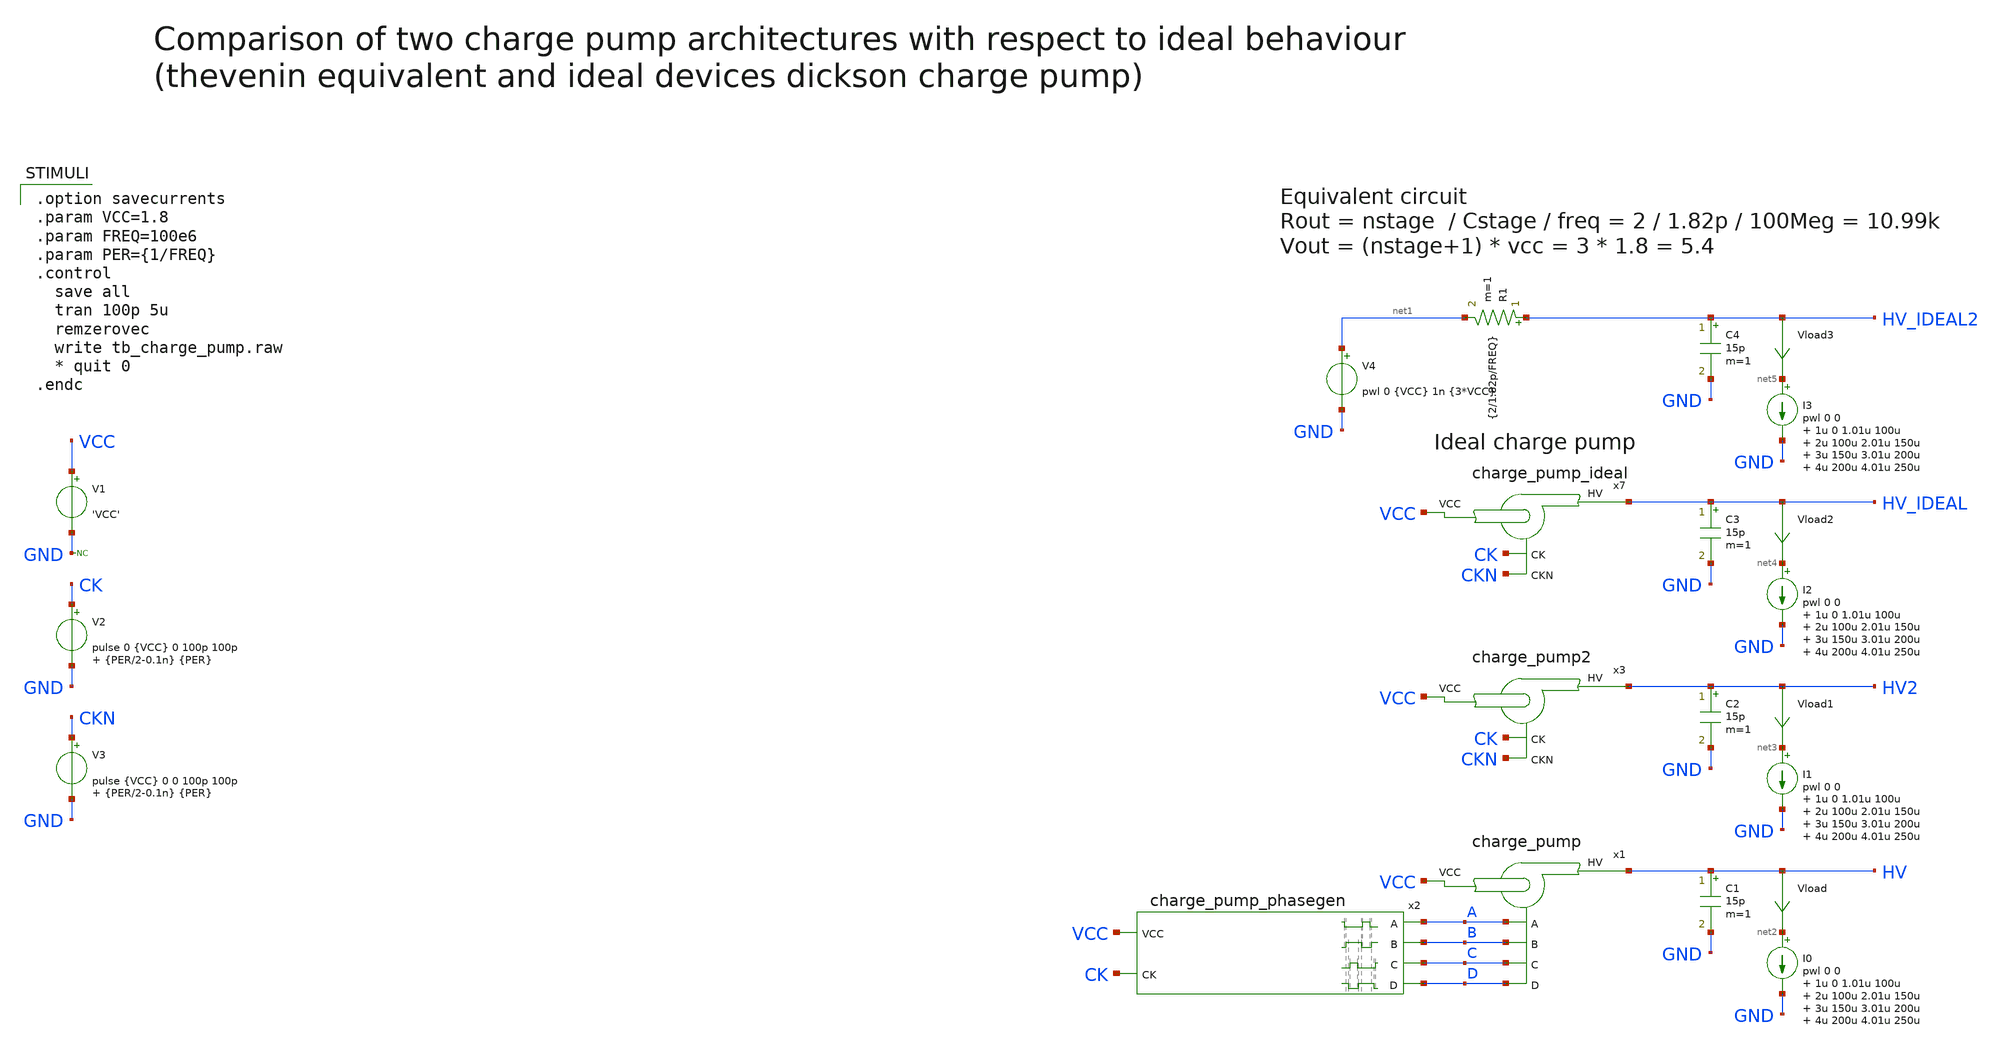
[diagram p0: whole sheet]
** sch_path: sky130_tests/tb_charge_pump.sch
* Copyright 2021 Stefan Frederik Schippers
* Licensed under the Apache License, Version 2.0 (the "License");
* you may not use this file except in compliance with the License.
* You may obtain a copy of the License at
* https://www.apache.org/licenses/LICENSE-2.0
* Unless required by applicable law or agreed to in writing, software
* distributed under the License is distributed on an "AS IS" BASIS,
* WITHOUT WARRANTIES OR CONDITIONS OF ANY KIND, either express or implied.
* See the License for the specific language governing permissions and
* limitations under the License.
* sky130_tests/lvtnot.sch:
* Copyright 2020 Stefan Frederik Schippers
.lib $::SKYWATER_MODELS/sky130.lib.spice tt
.include $::SKYWATER_STDCELLS/sky130_fd_sc_hd.spice

**.subckt tb_charge_pump
x1 VCC HV A B C D charge_pump
x2 A B C CK D VCC charge_pump_phasegen
V1 VCC GND 'VCC'
V2 CK GND pulse 0 {VCC} 0 100p 100p {PER/2-0.1n} {PER}
C1 HV GND 15p m=1
I0 net2 GND pwl 0 0 1u 0 1.01u 100u 2u 100u 2.01u 150u 3u 150u 3.01u 200u 4u 200u 4.01u 250u
Vload HV net2 0
.save i(vload)
x3 VCC HV2 CK CKN charge_pump2
V3 CKN GND pulse {VCC} 0 0 100p 100p {PER/2-0.1n} {PER}
C2 HV2 GND 15p m=1
I1 net3 GND pwl 0 0 1u 0 1.01u 100u 2u 100u 2.01u 150u 3u 150u 3.01u 200u 4u 200u 4.01u 250u
Vload1 HV2 net3 0
.save i(vload1)
* noconn GND
C3 HV_IDEAL GND 15p m=1
Vload2 HV_IDEAL net4 0
.save i(vload2)
x7 VCC HV_IDEAL CK CKN charge_pump_ideal
I2 net4 GND pwl 0 0 1u 0 1.01u 100u 2u 100u 2.01u 150u 3u 150u 3.01u 200u 4u 200u 4.01u 250u
V4 net1 GND pwl 0 {VCC} 1n {3*VCC}
R1 HV_IDEAL2 net1 {2/1.82p/FREQ} m=1
C4 HV_IDEAL2 GND 15p m=1
Vload3 HV_IDEAL2 net5 0
.save i(vload3)
I3 net5 GND pwl 0 0 1u 0 1.01u 100u 2u 100u 2.01u 150u 3u 150u 3.01u 200u 4u 200u 4.01u 250u
**** begin user architecture code

.option savecurrents
.param VCC=1.8
.param FREQ=100e6
.param PER={1/FREQ}
.control
  save all
  tran 100p 5u
  remzerovec
  write tb_charge_pump.raw
  * quit 0
.endc


**** end user architecture code
**.ends

* expanding   symbol:  sky130_tests/charge_pump.sym # of pins=6
** sym_path: sky130_tests/charge_pump.sym
** sch_path: sky130_tests/charge_pump.sch
.subckt charge_pump VCC HV A B C D
*.ipin A
*.ipin B
*.ipin C
*.ipin D
*.ipin VCC
*.iopin HV
XM1 net15 net9 net16 net5 sky130_fd_pr__nfet_g5v0d10v5 L=0.5 W=8 nf=1 ad='int((1 + 1)/2) * 8 / 1 * 0.29'
+ as='int((1 + 2)/2) * 8 / 1 * 0.29' pd='2*int((1 + 1)/2) * (8 / 1 + 0.29)' ps='2*int((1 + 2)/2) * (8 / 1 + 0.29)'
+ nrd='0.29 / 8 ' nrs='0.29 / 8 ' sa=0 sb=0 sd=0 mult=1 m=1
XM2 VCC HV1A G1A VCC sky130_fd_pr__nfet_g5v0d10v5 L=0.5 W=1.5 nf=1 ad='int((1 + 1)/2) * 1.5 / 1 * 0.29'
+ as='int((1 + 2)/2) * 1.5 / 1 * 0.29' pd='2*int((1 + 1)/2) * (1.5 / 1 + 0.29)' ps='2*int((1 + 2)/2) * (1.5 / 1 + 0.29)'
+ nrd='0.29 / 1.5 ' nrs='0.29 / 1.5 ' sa=0 sb=0 sd=0 mult=1 m=1
XM3 net1 net10 net17 net6 sky130_fd_pr__nfet_g5v0d10v5 L=0.5 W=8 nf=1 ad='int((1 + 1)/2) * 8 / 1 * 0.29'
+ as='int((1 + 2)/2) * 8 / 1 * 0.29' pd='2*int((1 + 1)/2) * (8 / 1 + 0.29)' ps='2*int((1 + 2)/2) * (8 / 1 + 0.29)'
+ nrd='0.29 / 8 ' nrs='0.29 / 8 ' sa=0 sb=0 sd=0 mult=1 m=1
XM4 HV1A HV2A G2A HV1A sky130_fd_pr__nfet_g5v0d10v5 L=0.5 W=1.5 nf=1 ad='int((1 + 1)/2) * 1.5 / 1 * 0.29'
+ as='int((1 + 2)/2) * 1.5 / 1 * 0.29' pd='2*int((1 + 1)/2) * (1.5 / 1 + 0.29)' ps='2*int((1 + 2)/2) * (1.5 / 1 + 0.29)'
+ nrd='0.29 / 1.5 ' nrs='0.29 / 1.5 ' sa=0 sb=0 sd=0 mult=1 m=1
XM5 HV2A net11 HV3A HV2A sky130_fd_pr__nfet_g5v0d10v5 L=0.5 W=1.5 nf=1 ad='int((1 + 1)/2) * 1.5 / 1 * 0.29'
+ as='int((1 + 2)/2) * 1.5 / 1 * 0.29' pd='2*int((1 + 1)/2) * (1.5 / 1 + 0.29)' ps='2*int((1 + 2)/2) * (1.5 / 1 + 0.29)'
+ nrd='0.29 / 1.5 ' nrs='0.29 / 1.5 ' sa=0 sb=0 sd=0 mult=1 m=1
XM6 HV2A HV3A G3A HV2A sky130_fd_pr__nfet_g5v0d10v5 L=0.5 W=1.5 nf=1 ad='int((1 + 1)/2) * 1.5 / 1 * 0.29'
+ as='int((1 + 2)/2) * 1.5 / 1 * 0.29' pd='2*int((1 + 1)/2) * (1.5 / 1 + 0.29)' ps='2*int((1 + 2)/2) * (1.5 / 1 + 0.29)'
+ nrd='0.29 / 1.5 ' nrs='0.29 / 1.5 ' sa=0 sb=0 sd=0 mult=1 m=1
XM7 HV2A G3A net3 HV2A sky130_fd_pr__nfet_g5v0d10v5 L=0.5 W=8 nf=1 ad='int((1 + 1)/2) * 8 / 1 * 0.29'
+ as='int((1 + 2)/2) * 8 / 1 * 0.29' pd='2*int((1 + 1)/2) * (8 / 1 + 0.29)' ps='2*int((1 + 2)/2) * (8 / 1 + 0.29)'
+ nrd='0.29 / 8 ' nrs='0.29 / 8 ' sa=0 sb=0 sd=0 mult=1 m=1
XC1 G1A A sky130_fd_pr__cap_mim_m3_1 W=6 L=4 MF=1 m=1
XC2 HV1A B sky130_fd_pr__cap_mim_m3_1 W=30 L=15 MF=1 m=1
XC3 G2A C sky130_fd_pr__cap_mim_m3_1 W=6 L=4 MF=1 m=1
XC4 HV2A D sky130_fd_pr__cap_mim_m3_1 W=30 L=15 MF=1 m=1
XC5 G3A A sky130_fd_pr__cap_mim_m3_1 W=6 L=4 MF=1 m=1
XC6 HV3A B sky130_fd_pr__cap_mim_m3_1 W=6 L=4 MF=1 m=1
XM8 net18 net12 net19 net7 sky130_fd_pr__nfet_g5v0d10v5 L=0.5 W=8 nf=1 ad='int((1 + 1)/2) * 8 / 1 * 0.29'
+ as='int((1 + 2)/2) * 8 / 1 * 0.29' pd='2*int((1 + 1)/2) * (8 / 1 + 0.29)' ps='2*int((1 + 2)/2) * (8 / 1 + 0.29)'
+ nrd='0.29 / 8 ' nrs='0.29 / 8 ' sa=0 sb=0 sd=0 mult=1 m=1
XM9 VCC HV1B G1B VCC sky130_fd_pr__nfet_g5v0d10v5 L=0.5 W=1.5 nf=1 ad='int((1 + 1)/2) * 1.5 / 1 * 0.29'
+ as='int((1 + 2)/2) * 1.5 / 1 * 0.29' pd='2*int((1 + 1)/2) * (1.5 / 1 + 0.29)' ps='2*int((1 + 2)/2) * (1.5 / 1 + 0.29)'
+ nrd='0.29 / 1.5 ' nrs='0.29 / 1.5 ' sa=0 sb=0 sd=0 mult=1 m=1
XM10 net2 net13 net20 net8 sky130_fd_pr__nfet_g5v0d10v5 L=0.5 W=8 nf=1 ad='int((1 + 1)/2) * 8 / 1 * 0.29'
+ as='int((1 + 2)/2) * 8 / 1 * 0.29' pd='2*int((1 + 1)/2) * (8 / 1 + 0.29)' ps='2*int((1 + 2)/2) * (8 / 1 + 0.29)'
+ nrd='0.29 / 8 ' nrs='0.29 / 8 ' sa=0 sb=0 sd=0 mult=1 m=1
XM11 HV1B HV2B G2B HV1B sky130_fd_pr__nfet_g5v0d10v5 L=0.5 W=1.5 nf=1 ad='int((1 + 1)/2) * 1.5 / 1 * 0.29'
+ as='int((1 + 2)/2) * 1.5 / 1 * 0.29' pd='2*int((1 + 1)/2) * (1.5 / 1 + 0.29)' ps='2*int((1 + 2)/2) * (1.5 / 1 + 0.29)'
+ nrd='0.29 / 1.5 ' nrs='0.29 / 1.5 ' sa=0 sb=0 sd=0 mult=1 m=1
XM12 HV2B net14 HV3B HV2B sky130_fd_pr__nfet_g5v0d10v5 L=0.5 W=1.5 nf=1 ad='int((1 + 1)/2) * 1.5 / 1 * 0.29'
+ as='int((1 + 2)/2) * 1.5 / 1 * 0.29' pd='2*int((1 + 1)/2) * (1.5 / 1 + 0.29)' ps='2*int((1 + 2)/2) * (1.5 / 1 + 0.29)'
+ nrd='0.29 / 1.5 ' nrs='0.29 / 1.5 ' sa=0 sb=0 sd=0 mult=1 m=1
XM13 HV2B HV3B G3B HV2B sky130_fd_pr__nfet_g5v0d10v5 L=0.5 W=1.5 nf=1 ad='int((1 + 1)/2) * 1.5 / 1 * 0.29'
+ as='int((1 + 2)/2) * 1.5 / 1 * 0.29' pd='2*int((1 + 1)/2) * (1.5 / 1 + 0.29)' ps='2*int((1 + 2)/2) * (1.5 / 1 + 0.29)'
+ nrd='0.29 / 1.5 ' nrs='0.29 / 1.5 ' sa=0 sb=0 sd=0 mult=1 m=1
XM14 HV2B G3B net4 HV2B sky130_fd_pr__nfet_g5v0d10v5 L=0.5 W=8 nf=1 ad='int((1 + 1)/2) * 8 / 1 * 0.29'
+ as='int((1 + 2)/2) * 8 / 1 * 0.29' pd='2*int((1 + 1)/2) * (8 / 1 + 0.29)' ps='2*int((1 + 2)/2) * (8 / 1 + 0.29)'
+ nrd='0.29 / 8 ' nrs='0.29 / 8 ' sa=0 sb=0 sd=0 mult=1 m=1
XC7 G1B C sky130_fd_pr__cap_mim_m3_1 W=6 L=4 MF=1 m=1
XC8 HV1B D sky130_fd_pr__cap_mim_m3_1 W=30 L=15 MF=1 m=1
XC9 G2B A sky130_fd_pr__cap_mim_m3_1 W=6 L=4 MF=1 m=1
XC10 HV2B B sky130_fd_pr__cap_mim_m3_1 W=30 L=15 MF=1 m=1
XC11 G3B C sky130_fd_pr__cap_mim_m3_1 W=6 L=4 MF=1 m=1
XC12 HV3B D sky130_fd_pr__cap_mim_m3_1 W=6 L=4 MF=1 m=1
V1 HV1B net2 0
.save i(v1)
V2 net3 HV 0
.save i(v2)
V3 net4 HV 0
.save i(v3)
V4 HV1A net1 0
.save i(v4)
V5 VCC net18 0
.save i(v5)
V6 VCC net15 0
.save i(v6)
V7 net20 HV2B 0
.save i(v7)
V8 net17 HV2A 0
.save i(v8)
V9 VCC net5 0
.save i(v9)
V10 HV1A net6 0
.save i(v10)
V11 VCC net7 0
.save i(v11)
V12 HV1B net8 0
.save i(v12)
V13 net19 HV1B 0
.save i(v13)
V14 net16 HV1A 0
.save i(v14)
V15 G1A net9 0
.save i(v15)
V16 G2A net10 0
.save i(v16)
V17 G3A net11 0
.save i(v17)
V18 G1B net12 0
.save i(v18)
V19 G2B net13 0
.save i(v19)
V20 G3B net14 0
.save i(v20)
.ends


* expanding   symbol:  sky130_tests/charge_pump_phasegen.sym # of pins=6
** sym_path: sky130_tests/charge_pump_phasegen.sym
** sch_path: sky130_tests/charge_pump_phasegen.sch
.subckt charge_pump_phasegen A B C CK D VCC
*.ipin CK
*.opin A
*.opin B
*.opin C
*.opin D
*.ipin VCC
x1 CKN BN GND GND VCC VCC AN sky130_fd_sc_hd__nand2_2
x2 AN GND GND VCC VCC A sky130_fd_sc_hd__inv_4
x5 AN CK GND GND VCC VCC net1 sky130_fd_sc_hd__nand2_1
x6 net1 net2 GND GND VCC VCC net5 sky130_fd_sc_hd__nand2_1
x7 net6 DI VCC GND lvtnot W_N=0.5 L_N=1 W_P=1 L_P=1 m=1
x8 net2 net6 VCC GND lvtnot W_N=0.5 L_N=1 W_P=1 L_P=1 m=1
x9 BN GND GND VCC VCC B sky130_fd_sc_hd__inv_12
x10 net5 GND GND VCC VCC BN sky130_fd_sc_hd__inv_2
x11 CK DN GND GND VCC VCC CN sky130_fd_sc_hd__nand2_2
x12 CN GND GND VCC VCC C sky130_fd_sc_hd__inv_4
x13 CN CKN GND GND VCC VCC net3 sky130_fd_sc_hd__nand2_1
x14 net3 net4 GND GND VCC VCC net7 sky130_fd_sc_hd__nand2_1
x15 net8 BI VCC GND lvtnot W_N=0.5 L_N=1 W_P=1 L_P=1 m=1
x16 net4 net8 VCC GND lvtnot W_N=0.5 L_N=1 W_P=1 L_P=1 m=1
x17 DN GND GND VCC VCC D sky130_fd_sc_hd__inv_12
x18 net7 GND GND VCC VCC DN sky130_fd_sc_hd__inv_2
x3 CK GND GND VCC VCC CKN sky130_fd_sc_hd__inv_12
* noconn VCC
x19 BN GND GND VCC VCC BI sky130_fd_sc_hd__inv_2
x20 DN GND GND VCC VCC DI sky130_fd_sc_hd__inv_2
.ends


* expanding   symbol:  sky130_tests/charge_pump2.sym # of pins=4
** sym_path: sky130_tests/charge_pump2.sym
** sch_path: sky130_tests/charge_pump2.sch
.subckt charge_pump2 VCC HV CK CKN
*.ipin VCC
*.iopin HV
*.ipin CK
*.ipin CKN
XM8 D1 GN1 VCC VCC sky130_fd_pr__nfet_g5v0d10v5 L=0.5 W=8 nf=1 ad='int((1 + 1)/2) * 8 / 1 * 0.29' as='int((1 + 2)/2) * 8 / 1 * 0.29'
+ pd='2*int((1 + 1)/2) * (8 / 1 + 0.29)' ps='2*int((1 + 2)/2) * (8 / 1 + 0.29)' nrd='0.29 / 8 ' nrs='0.29 / 8 '
+ sa=0 sb=0 sd=0 mult=1 m=1
XM9 D2 GN2 VCC VCC sky130_fd_pr__nfet_g5v0d10v5 L=0.5 W=8 nf=1 ad='int((1 + 1)/2) * 8 / 1 * 0.29' as='int((1 + 2)/2) * 8 / 1 * 0.29'
+ pd='2*int((1 + 1)/2) * (8 / 1 + 0.29)' ps='2*int((1 + 2)/2) * (8 / 1 + 0.29)' nrd='0.29 / 8 ' nrs='0.29 / 8 '
+ sa=0 sb=0 sd=0 mult=1 m=1
XM10 D1 GP1 HV1 HV1 sky130_fd_pr__pfet_g5v0d10v5 L=0.5 W=16 nf=1 ad='int((1 + 1)/2) * 16 / 1 * 0.29'
+ as='int((1 + 2)/2) * 16 / 1 * 0.29' pd='2*int((1 + 1)/2) * (16 / 1 + 0.29)' ps='2*int((1 + 2)/2) * (16 / 1 + 0.29)'
+ nrd='0.29 / 16 ' nrs='0.29 / 16 ' sa=0 sb=0 sd=0 mult=1 m=1
XM11 D2 GP2 HV1 HV1 sky130_fd_pr__pfet_g5v0d10v5 L=0.5 W=16 nf=1 ad='int((1 + 1)/2) * 16 / 1 * 0.29'
+ as='int((1 + 2)/2) * 16 / 1 * 0.29' pd='2*int((1 + 1)/2) * (16 / 1 + 0.29)' ps='2*int((1 + 2)/2) * (16 / 1 + 0.29)'
+ nrd='0.29 / 16 ' nrs='0.29 / 16 ' sa=0 sb=0 sd=0 mult=1 m=1
XC7 D2 net1 sky130_fd_pr__cap_mim_m3_1 W=30 L=15 MF=1 m=1
XC8 D1 net2 sky130_fd_pr__cap_mim_m3_1 W=30 L=15 MF=1 m=1
XM12 D3 GN3 HV1 HV1 sky130_fd_pr__nfet_g5v0d10v5 L=0.5 W=8 nf=1 ad='int((1 + 1)/2) * 8 / 1 * 0.29' as='int((1 + 2)/2) * 8 / 1 * 0.29'
+ pd='2*int((1 + 1)/2) * (8 / 1 + 0.29)' ps='2*int((1 + 2)/2) * (8 / 1 + 0.29)' nrd='0.29 / 8 ' nrs='0.29 / 8 '
+ sa=0 sb=0 sd=0 mult=1 m=1
XM13 D4 GN4 HV1 HV1 sky130_fd_pr__nfet_g5v0d10v5 L=0.5 W=8 nf=1 ad='int((1 + 1)/2) * 8 / 1 * 0.29' as='int((1 + 2)/2) * 8 / 1 * 0.29'
+ pd='2*int((1 + 1)/2) * (8 / 1 + 0.29)' ps='2*int((1 + 2)/2) * (8 / 1 + 0.29)' nrd='0.29 / 8 ' nrs='0.29 / 8 '
+ sa=0 sb=0 sd=0 mult=1 m=1
XM14 D3 GP3 HV HV sky130_fd_pr__pfet_g5v0d10v5 L=0.5 W=16 nf=1 ad='int((1 + 1)/2) * 16 / 1 * 0.29' as='int((1 + 2)/2) * 16 / 1 * 0.29'
+ pd='2*int((1 + 1)/2) * (16 / 1 + 0.29)' ps='2*int((1 + 2)/2) * (16 / 1 + 0.29)' nrd='0.29 / 16 ' nrs='0.29 / 16 '
+ sa=0 sb=0 sd=0 mult=1 m=1
XM15 D4 GP4 HV HV sky130_fd_pr__pfet_g5v0d10v5 L=0.5 W=16 nf=1 ad='int((1 + 1)/2) * 16 / 1 * 0.29' as='int((1 + 2)/2) * 16 / 1 * 0.29'
+ pd='2*int((1 + 1)/2) * (16 / 1 + 0.29)' ps='2*int((1 + 2)/2) * (16 / 1 + 0.29)' nrd='0.29 / 16 ' nrs='0.29 / 16 '
+ sa=0 sb=0 sd=0 mult=1 m=1
XC9 D4 net3 sky130_fd_pr__cap_mim_m3_1 W=30 L=15 MF=1 m=1
XC10 D3 net4 sky130_fd_pr__cap_mim_m3_1 W=30 L=15 MF=1 m=1
x12 CK GND GND VCC VCC net1 sky130_fd_sc_hd__inv_6
x1 CKN GND GND VCC VCC net2 sky130_fd_sc_hd__inv_6
x2 CK GND GND VCC VCC net3 sky130_fd_sc_hd__inv_6
x3 CKN GND GND VCC VCC net4 sky130_fd_sc_hd__inv_6
XM1 GP3 GP4 HV HV sky130_fd_pr__pfet_g5v0d10v5 L=0.5 W=1 nf=1 ad='int((1 + 1)/2) * 1 / 1 * 0.29' as='int((1 + 2)/2) * 1 / 1 * 0.29'
+ pd='2*int((1 + 1)/2) * (1 / 1 + 0.29)' ps='2*int((1 + 2)/2) * (1 / 1 + 0.29)' nrd='0.29 / 1 ' nrs='0.29 / 1 '
+ sa=0 sb=0 sd=0 mult=1 m=1
XM2 GP4 GP3 HV HV sky130_fd_pr__pfet_g5v0d10v5 L=0.5 W=1 nf=1 ad='int((1 + 1)/2) * 1 / 1 * 0.29' as='int((1 + 2)/2) * 1 / 1 * 0.29'
+ pd='2*int((1 + 1)/2) * (1 / 1 + 0.29)' ps='2*int((1 + 2)/2) * (1 / 1 + 0.29)' nrd='0.29 / 1 ' nrs='0.29 / 1 '
+ sa=0 sb=0 sd=0 mult=1 m=1
XC1 GP3 net5 sky130_fd_pr__cap_mim_m3_1 W=6 L=8 MF=1 m=1
XC2 GP4 net6 sky130_fd_pr__cap_mim_m3_1 W=6 L=8 MF=1 m=1
XM3 GP1 GP2 HV1 HV1 sky130_fd_pr__pfet_g5v0d10v5 L=0.5 W=1 nf=1 ad='int((1 + 1)/2) * 1 / 1 * 0.29' as='int((1 + 2)/2) * 1 / 1 * 0.29'
+ pd='2*int((1 + 1)/2) * (1 / 1 + 0.29)' ps='2*int((1 + 2)/2) * (1 / 1 + 0.29)' nrd='0.29 / 1 ' nrs='0.29 / 1 '
+ sa=0 sb=0 sd=0 mult=1 m=1
XM4 GP2 GP1 HV1 HV1 sky130_fd_pr__pfet_g5v0d10v5 L=0.5 W=1 nf=1 ad='int((1 + 1)/2) * 1 / 1 * 0.29' as='int((1 + 2)/2) * 1 / 1 * 0.29'
+ pd='2*int((1 + 1)/2) * (1 / 1 + 0.29)' ps='2*int((1 + 2)/2) * (1 / 1 + 0.29)' nrd='0.29 / 1 ' nrs='0.29 / 1 '
+ sa=0 sb=0 sd=0 mult=1 m=1
XC3 GP1 net7 sky130_fd_pr__cap_mim_m3_1 W=6 L=8 MF=1 m=1
XC4 GP2 net8 sky130_fd_pr__cap_mim_m3_1 W=6 L=8 MF=1 m=1
x4 CK GND GND VCC VCC net5 sky130_fd_sc_hd__inv_2
x5 CKN GND GND VCC VCC net6 sky130_fd_sc_hd__inv_2
x6 CK GND GND VCC VCC net7 sky130_fd_sc_hd__inv_2
x7 CKN GND GND VCC VCC net8 sky130_fd_sc_hd__inv_2
XC5 GN1 net9 sky130_fd_pr__cap_mim_m3_1 W=6 L=4 MF=1 m=1
XC6 GN2 net10 sky130_fd_pr__cap_mim_m3_1 W=6 L=4 MF=1 m=1
x8 CK GND GND VCC VCC net9 sky130_fd_sc_hd__inv_2
x9 CKN GND GND VCC VCC net10 sky130_fd_sc_hd__inv_2
XM5 VCC GN1 GN2 VCC sky130_fd_pr__nfet_g5v0d10v5 L=0.5 W=0.5 nf=1 ad='int((1 + 1)/2) * 0.5 / 1 * 0.29'
+ as='int((1 + 2)/2) * 0.5 / 1 * 0.29' pd='2*int((1 + 1)/2) * (0.5 / 1 + 0.29)' ps='2*int((1 + 2)/2) * (0.5 / 1 + 0.29)'
+ nrd='0.29 / 0.5 ' nrs='0.29 / 0.5 ' sa=0 sb=0 sd=0 mult=1 m=1
XM6 VCC GN2 GN1 VCC sky130_fd_pr__nfet_g5v0d10v5 L=0.5 W=0.5 nf=1 ad='int((1 + 1)/2) * 0.5 / 1 * 0.29'
+ as='int((1 + 2)/2) * 0.5 / 1 * 0.29' pd='2*int((1 + 1)/2) * (0.5 / 1 + 0.29)' ps='2*int((1 + 2)/2) * (0.5 / 1 + 0.29)'
+ nrd='0.29 / 0.5 ' nrs='0.29 / 0.5 ' sa=0 sb=0 sd=0 mult=1 m=1
XC11 GN3 net11 sky130_fd_pr__cap_mim_m3_1 W=6 L=4 MF=1 m=1
XC12 GN4 net12 sky130_fd_pr__cap_mim_m3_1 W=6 L=4 MF=1 m=1
x10 CK GND GND VCC VCC net11 sky130_fd_sc_hd__inv_2
x11 CKN GND GND VCC VCC net12 sky130_fd_sc_hd__inv_2
XM7 HV1 GN3 GN4 HV1 sky130_fd_pr__nfet_g5v0d10v5 L=0.5 W=0.5 nf=1 ad='int((1 + 1)/2) * 0.5 / 1 * 0.29'
+ as='int((1 + 2)/2) * 0.5 / 1 * 0.29' pd='2*int((1 + 1)/2) * (0.5 / 1 + 0.29)' ps='2*int((1 + 2)/2) * (0.5 / 1 + 0.29)'
+ nrd='0.29 / 0.5 ' nrs='0.29 / 0.5 ' sa=0 sb=0 sd=0 mult=1 m=1
XM16 HV1 GN4 GN3 HV1 sky130_fd_pr__nfet_g5v0d10v5 L=0.5 W=0.5 nf=1 ad='int((1 + 1)/2) * 0.5 / 1 * 0.29'
+ as='int((1 + 2)/2) * 0.5 / 1 * 0.29' pd='2*int((1 + 1)/2) * (0.5 / 1 + 0.29)' ps='2*int((1 + 2)/2) * (0.5 / 1 + 0.29)'
+ nrd='0.29 / 0.5 ' nrs='0.29 / 0.5 ' sa=0 sb=0 sd=0 mult=1 m=1
.ends


* expanding   symbol:  sky130_tests/charge_pump_ideal.sym # of pins=4
** sym_path: sky130_tests/charge_pump_ideal.sym
** sch_path: sky130_tests/charge_pump_ideal.sch
.subckt charge_pump_ideal VCC HV CK CKN
*.iopin HV
*.ipin VCC
*.ipin CK
*.ipin CKN
X4 net2 HV diode_ngspice Ron=0.1 Roff=1e9 m=1
X5 net1 net2 diode_ngspice Ron=0.1 Roff=1e9 m=1
X6 VCC net1 diode_ngspice Ron=0.1 Roff=1e9 m=1
C1 net2 CKNI 1.82p m=1
C2 net1 CKI 1.82p m=1
S1 CKNI GND CK GND SW1
S2 VCC CKNI VCC CK SW1
S3 CKI GND CKN GND SW1
S4 VCC CKI VCC CKN SW1
C3 CKI 0 50f m=1
C4 CKNI 0 50f m=1
.ends


* expanding   symbol:  sky130_tests/lvtnot.sym # of pins=2
** sym_path: sky130_tests/lvtnot.sym
** sch_path: sky130_tests/lvtnot.sch
.subckt lvtnot y a VCCPIN VSSPIN     W_N=1 L_N=0.15 W_P=2 L_P=0.35
*.opin y
*.ipin a
XM1 y a VSSPIN VSSPIN sky130_fd_pr__nfet_01v8_lvt L=L_N W=W_N nf=1 ad='int((1 + 1)/2) * W_N / 1 * 0.29'
+ as='int((1 + 2)/2) * W_N / 1 * 0.29' pd='2*int((1 + 1)/2) * (W_N / 1 + 0.29)' ps='2*int((1 + 2)/2) * (W_N / 1 + 0.29)'
+ nrd='0.29 / W_N ' nrs='0.29 / W_N ' sa=0 sb=0 sd=0 mult=1 m=1
XM2 y a VCCPIN VCCPIN sky130_fd_pr__pfet_01v8_lvt L=L_P W=W_P nf=1 ad='int((1 + 1)/2) * W_P / 1 * 0.29'
+ as='int((1 + 2)/2) * W_P / 1 * 0.29' pd='2*int((1 + 1)/2) * (W_P / 1 + 0.29)' ps='2*int((1 + 2)/2) * (W_P / 1 + 0.29)'
+ nrd='0.29 / W_P ' nrs='0.29 / W_P ' sa=0 sb=0 sd=0 mult=1 m=1
.ends


* expanding   symbol:  sky130_tests/diode_ngspice.sym # of pins=2
** sym_path: sky130_tests/diode_ngspice.sym
** sch_path: sky130_tests/diode_ngspice.sch
.subckt diode_ngspice plus minus   Roff=1e9 Ron=0.1
*.iopin plus
*.iopin minus
Vm mn minus 0
.save i(vm)
Vp plus pn 0
.save i(vp)
B1 pn mn I = 'v(pn,mn) > 0 ? v(pn,mn) / Ron : v(pn,mn) / Roff'
.ends

**** begin user architecture code
.MODEL SW1 SW   VT=1.0 VH=0.01  RON=10 ROFF=10MEG
**** end user architecture code
.end
